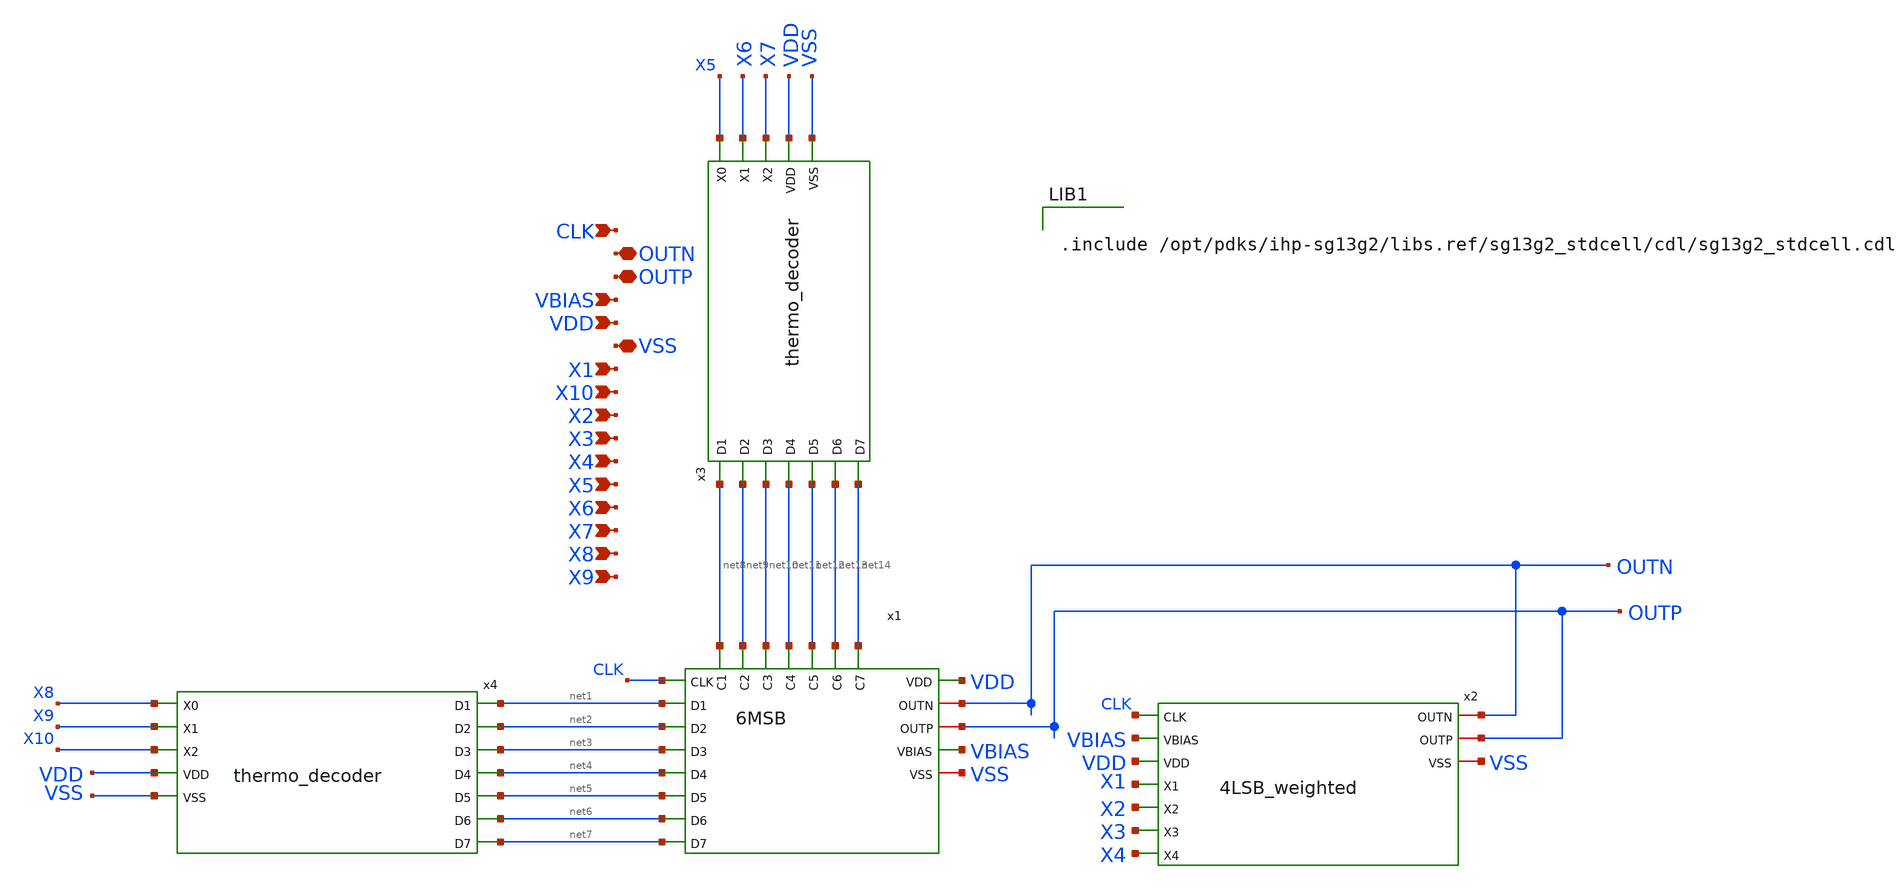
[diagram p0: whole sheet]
** sch_path: dependencies/DAC/dependencies/CS_DAC-/xschem/CS_DAC_10b.sch
**.subckt CS_DAC_10b X9 X8 X7 X6 X5 X4 X3 X2 X10 X1 VSS VDD VBIAS OUTP OUTN CLK
*.ipin X9
*.ipin X8
*.ipin X7
*.ipin X6
*.ipin X5
*.ipin X4
*.ipin X3
*.ipin X2
*.ipin X10
*.ipin X1
*.iopin VSS
*.ipin VDD
*.ipin VBIAS
*.iopin OUTP
*.iopin OUTN
*.ipin CLK
x3 net8 net9 net10 net11 net12 net13 net14 X5 X6 X7 VDD VSS thermo_decoder
x4 net1 net2 net3 net4 net5 net6 net7 X8 X9 X10 VDD VSS thermo_decoder
x1 net8 net9 net10 net11 net12 net13 net14 CLK net1 net2 net3 net4 net5 net6 net7 OUTN OUTP VBIAS
+ VDD VSS 6MSB
x2 CLK OUTN OUTP VBIAS VDD VSS X1 X2 X3 X4 4LSB_weighted
**** begin user architecture code


.include /opt/pdks/ihp-sg13g2/libs.ref/sg13g2_stdcell/cdl/sg13g2_stdcell.cdl



**** end user architecture code
**.ends
.end
